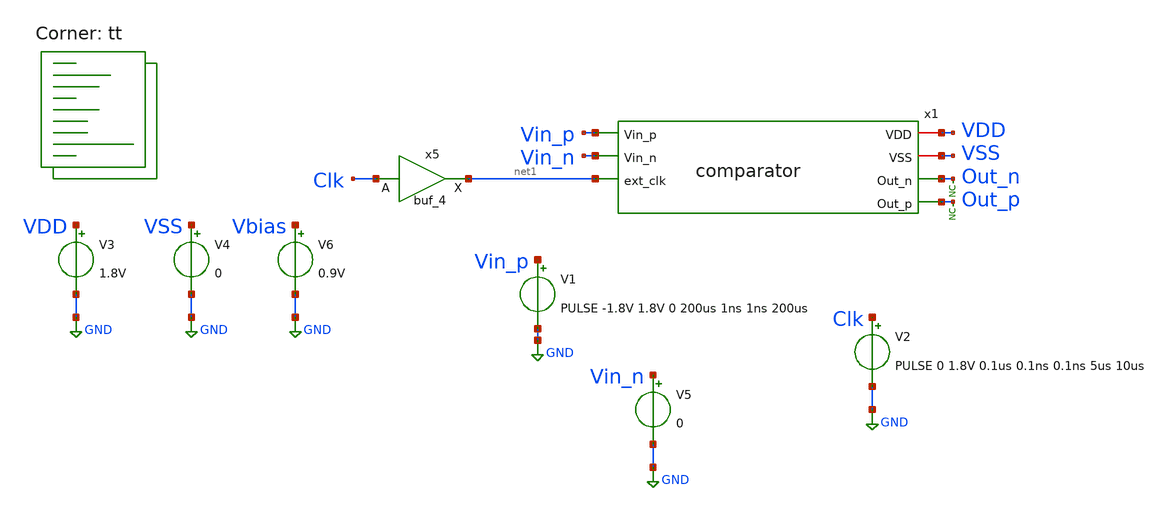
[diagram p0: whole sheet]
** sch_path: xschem/tests/comparator/comparator_test_sub_cm.sch
**.subckt comparator_test_sub_cm
V3 VDD GND 1.8V
V4 VSS GND 0
x1 VDD VSS Vin_p Out_n Vin_n Out_p net1 comparator
V1 Vin_p GND PULSE -1.8V 1.8V 0 200us 1ns 1ns 200us
V2 Clk GND PULSE 0 1.8V 0.1us 0.1ns 0.1ns 5us 10us
* noconn Out_p
* noconn Out_n
V6 Vbias GND 0.9V
x5 Clk VSS VSS VDD VDD net1 sky130_fd_sc_hd__buf_4
V5 Vin_n GND 0
**** begin user architecture code
 *.lib $::SKYWATER_MODELS/sky130.lib.spice tt
.include $::SKYWATER_STDCELLS/sky130_fd_sc_hd.spice



* Here's a comment
.options acct list
.options method=gear
.temp 25
*vvcc VDD 0 dc 1.8
*vvss VSS 0 0
.control
save all
tran 0.1u 200u
*dc V1 0 1.8V 0.1
plot Vin_p-Vin_n Out_p-Out_n Clk-4
* plot Vbias Vin_p Vin_n
plot x1.pre_amp_p x1.pre_amp_n+2 clk-2
*plot i(v.x1.v1) i(v.x1.v2)+2 clk-2
plot Vin_p-Vin_n x1.pre_amp_p-x1.pre_amp_n Out_p-Out_n+4 Clk-4
plot Vin_p-Vin_n x1.pre_amp_p-x1.pre_amp_n
plot Vin_p-Vin_n x1.pre_amp_p-x1.pre_amp_n out_p-out_n
write comparator_test_small_v.raw
.endc


.lib $::SKYWATER_MODELS/sky130.lib.spice tt
**** end user architecture code
**.ends

* expanding   symbol:  src/comparator/comparator.sym # of pins=7
** sym_path: src/comparator/comparator.sym
** sch_path: src/comparator/comparator.sch
.subckt comparator VDD VSS Vin_p Out_n Vin_n Out_p ext_clk
*.iopin VDD
*.iopin VSS
*.ipin Vin_p
*.opin Out_n
*.ipin Vin_n
*.opin Out_p
*.ipin ext_clk
XM1 Pre_Amp_p Clk_n VDD VDD sky130_fd_pr__pfet_01v8 L=0.15 W=5 nf=1 ad='int((nf+1)/2) * W/nf * 0.29' as='int((nf+2)/2)
+ * W/nf * 0.29' pd='2*int((nf+1)/2) * (W/nf + 0.29)' ps='2*int((nf+2)/2) * (W/nf + 0.29)' nrd='0.29 /
+ W' nrs='0.29 / W' sa=0 sb=0 sd=0 mult=2 m=2
XM2 Pre_Amp_n Clk_n VDD VDD sky130_fd_pr__pfet_01v8 L=0.15 W=5 nf=1 ad='int((nf+1)/2) * W/nf * 0.29' as='int((nf+2)/2)
+ * W/nf * 0.29' pd='2*int((nf+1)/2) * (W/nf + 0.29)' ps='2*int((nf+2)/2) * (W/nf + 0.29)' nrd='0.29 /
+ W' nrs='0.29 / W' sa=0 sb=0 sd=0 mult=2 m=2
XM3 Pre_Amp_n Vin_p net1 VSS sky130_fd_pr__nfet_01v8 L=0.15 W=5 nf=1 ad='int((nf+1)/2) * W/nf * 0.29' as='int((nf+2)/2)
+ * W/nf * 0.29' pd='2*int((nf+1)/2) * (W/nf + 0.29)' ps='2*int((nf+2)/2) * (W/nf + 0.29)' nrd='0.29 /
+ W' nrs='0.29 / W' sa=0 sb=0 sd=0 mult=10 m=10
XM4 Pre_Amp_p Vin_n net1 VSS sky130_fd_pr__nfet_01v8 L=0.15 W=5 nf=1 ad='int((nf+1)/2) * W/nf * 0.29' as='int((nf+2)/2)
+ * W/nf * 0.29' pd='2*int((nf+1)/2) * (W/nf + 0.29)' ps='2*int((nf+2)/2) * (W/nf + 0.29)' nrd='0.29 /
+ W' nrs='0.29 / W' sa=0 sb=0 sd=0 mult=10 m=10
XM5 net3 net5 VDD VDD sky130_fd_pr__pfet_01v8 L=0.15 W=1.605 nf=1 ad='int((nf+1)/2) * W/nf * 0.29' as='int((nf+2)/2)
+ * W/nf * 0.29' pd='2*int((nf+1)/2) * (W/nf + 0.29)' ps='2*int((nf+2)/2) * (W/nf + 0.29)' nrd='0.29 /
+ W' nrs='0.29 / W' sa=0 sb=0 sd=0 mult=4 m=4
XM6 net2 net4 VDD VDD sky130_fd_pr__pfet_01v8 L=0.15 W=1.605 nf=1 ad='int((nf+1)/2) * W/nf * 0.29' as='int((nf+2)/2)
+ * W/nf * 0.29' pd='2*int((nf+1)/2) * (W/nf + 0.29)' ps='2*int((nf+2)/2) * (W/nf + 0.29)' nrd='0.29 /
+ W' nrs='0.29 / W' sa=0 sb=0 sd=0 mult=4 m=4
XM9 net1 Clk VSS VSS sky130_fd_pr__nfet_01v8 L=0.15 W=50 nf=5 ad='int((nf+1)/2) * W/nf * 0.29' as='int((nf+2)/2)
+ * W/nf * 0.29' pd='2*int((nf+1)/2) * (W/nf + 0.29)' ps='2*int((nf+2)/2) * (W/nf + 0.29)' nrd='0.29 /
+ W' nrs='0.29 / W' sa=0 sb=0 sd=0 mult=1 m=1
XM11 net4 Clk_latch_n VSS VSS sky130_fd_pr__nfet_01v8 L=0.15 W=0.91 nf=1 ad='int((nf+1)/2) * W/nf * 0.29' as='int((nf+2)/2)
+ * W/nf * 0.29' pd='2*int((nf+1)/2) * (W/nf + 0.29)' ps='2*int((nf+2)/2) * (W/nf + 0.29)' nrd='0.29 /
+ W' nrs='0.29 / W' sa=0 sb=0 sd=0 mult=4 m=4
XM12 net4 net5 VSS VSS sky130_fd_pr__nfet_01v8 L=0.15 W=0.91 nf=1 ad='int((nf+1)/2) * W/nf * 0.29' as='int((nf+2)/2)
+ * W/nf * 0.29' pd='2*int((nf+1)/2) * (W/nf + 0.29)' ps='2*int((nf+2)/2) * (W/nf + 0.29)' nrd='0.29 /
+ W' nrs='0.29 / W' sa=0 sb=0 sd=0 mult=4 m=4
XM13 net5 net4 VSS VSS sky130_fd_pr__nfet_01v8 L=0.15 W=0.91 nf=1 ad='int((nf+1)/2) * W/nf * 0.29' as='int((nf+2)/2)
+ * W/nf * 0.29' pd='2*int((nf+1)/2) * (W/nf + 0.29)' ps='2*int((nf+2)/2) * (W/nf + 0.29)' nrd='0.29 /
+ W' nrs='0.29 / W' sa=0 sb=0 sd=0 mult=4 m=4
XM14 net5 Clk_latch_n VSS VSS sky130_fd_pr__nfet_01v8 L=0.15 W=0.91 nf=1 ad='int((nf+1)/2) * W/nf * 0.29' as='int((nf+2)/2)
+ * W/nf * 0.29' pd='2*int((nf+1)/2) * (W/nf + 0.29)' ps='2*int((nf+2)/2) * (W/nf + 0.29)' nrd='0.29 /
+ W' nrs='0.29 / W' sa=0 sb=0 sd=0 mult=4 m=4
XM7 net5 Pre_Amp_n net2 VDD sky130_fd_pr__pfet_01v8 L=0.15 W=1.605 nf=1 ad='int((nf+1)/2) * W/nf * 0.29' as='int((nf+2)/2)
+ * W/nf * 0.29' pd='2*int((nf+1)/2) * (W/nf + 0.29)' ps='2*int((nf+2)/2) * (W/nf + 0.29)' nrd='0.29 /
+ W' nrs='0.29 / W' sa=0 sb=0 sd=0 mult=8 m=8
XM8 net4 Pre_Amp_p net3 VDD sky130_fd_pr__pfet_01v8 L=0.15 W=1.605 nf=1 ad='int((nf+1)/2) * W/nf * 0.29' as='int((nf+2)/2)
+ * W/nf * 0.29' pd='2*int((nf+1)/2) * (W/nf + 0.29)' ps='2*int((nf+2)/2) * (W/nf + 0.29)' nrd='0.29 /
+ W' nrs='0.29 / W' sa=0 sb=0 sd=0 mult=8 m=8
x1 net4 VSS VSS VDD VDD net6 sky130_fd_sc_hd__buf_1
x2 net6 VSS VSS VDD VDD net7 sky130_fd_sc_hd__buf_4
x3 net7 VSS VSS VDD VDD Out_n sky130_fd_sc_hd__buf_8
x4 net5 VSS VSS VDD VDD net8 sky130_fd_sc_hd__buf_1
x5 net8 VSS VSS VDD VDD net9 sky130_fd_sc_hd__buf_4
x6 net9 VSS VSS VDD VDD Out_p sky130_fd_sc_hd__buf_8
x7 ext_clk VSS VSS VDD VDD net10 sky130_fd_sc_hd__buf_1
x8 net17 VSS VSS VDD VDD net14 sky130_fd_sc_hd__clkdlybuf4s15_1
x9 net11 VSS VSS VDD VDD Clk_latch_n sky130_fd_sc_hd__buf_2
x10 net14 VSS VSS VDD VDD net15 sky130_fd_sc_hd__clkdlybuf4s15_1
x11 net15 VSS VSS VDD VDD net11 sky130_fd_sc_hd__clkdlybuf4s50_1
x13 Clk VSS VSS VDD VDD net12 sky130_fd_sc_hd__inv_2
x12 net10 VSS VSS VDD VDD net13 sky130_fd_sc_hd__buf_2
x14 net13 VSS VSS VDD VDD net16 sky130_fd_sc_hd__buf_4
x15 net16 VSS VSS VDD VDD Clk sky130_fd_sc_hd__buf_8
x16 net12 VSS VSS VDD VDD Clk_n sky130_fd_sc_hd__buf_4
x17 Clk VSS VSS VDD VDD net17 sky130_fd_sc_hd__inv_2
.ends

.GLOBAL GND
.end
